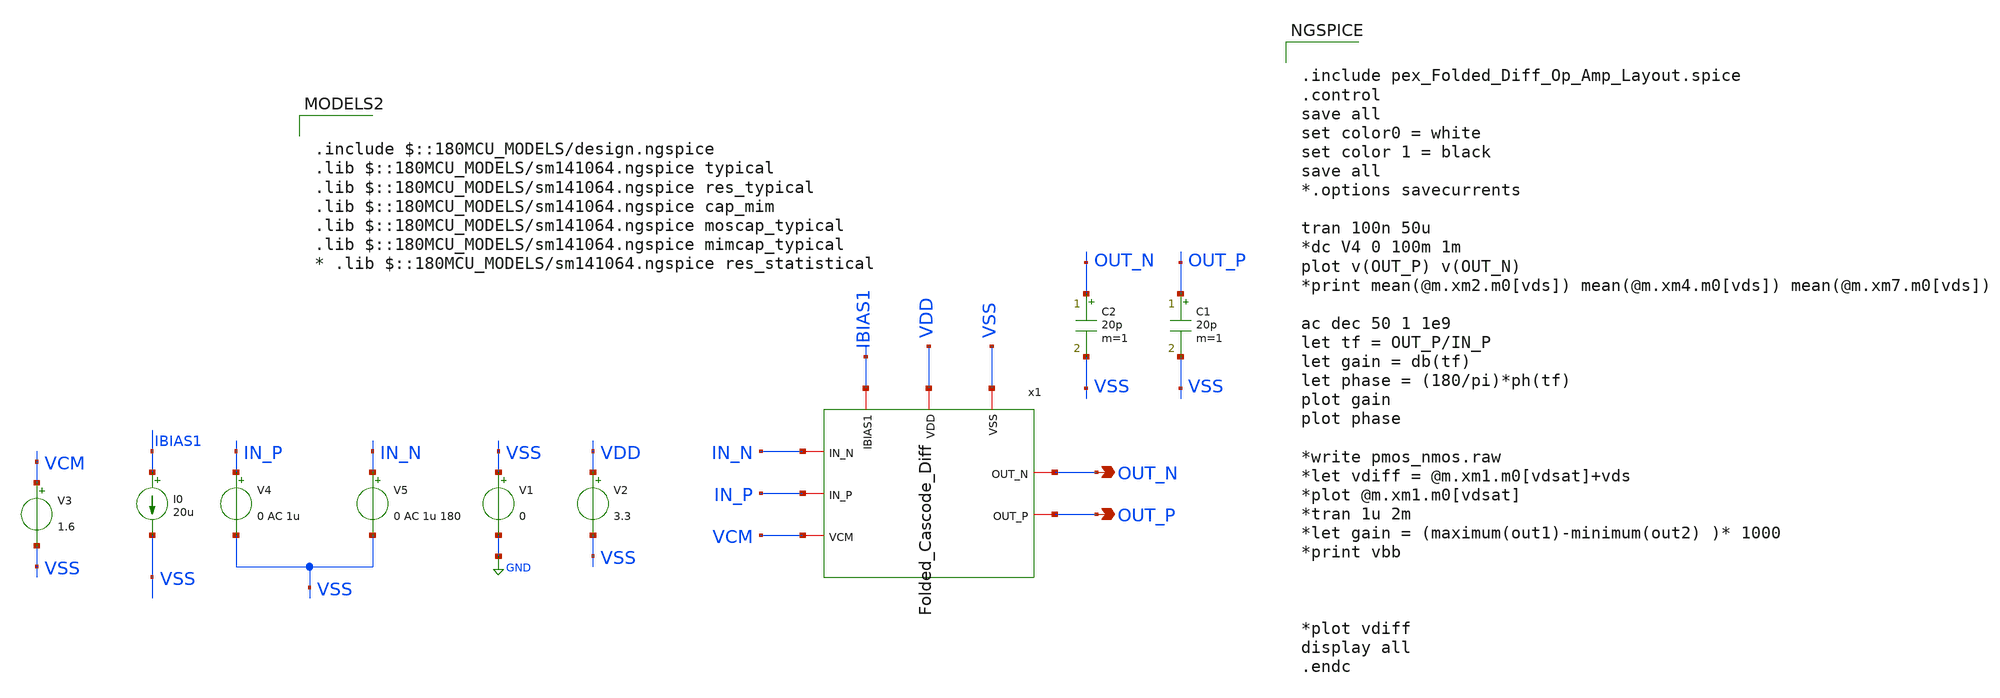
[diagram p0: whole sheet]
** sch_path: AWG_OUTPUT_AND_MUX_PAKISTAN_05/xschem/Folded_Cascode_Diff_TB_Sch.sch
**.subckt Folded_Cascode_Diff_TB_Sch OUT_N OUT_P
*.opin OUT_N
*.opin OUT_P
V1 VSS GND 0
V2 VDD VSS 3.3
V3 VCM VSS 1.6
I0 IBIAS1 VSS 20u
V4 IN_P VSS 0 AC 1u
V5 IN_N VSS 0 AC 1u 180
C1 OUT_P VSS 20p m=1
C2 OUT_N VSS 20p m=1
x1 VDD VSS IN_N IN_P IBIAS1 VCM OUT_N OUT_P Folded_Cascode_Diff
**** begin user architecture code


.include pex_Folded_Diff_Op_Amp_Layout.spice
.control
save all
set color0 = white
set color 1 = black
save all
*.options savecurrents

tran 100n 50u
*dc V4 0 100m 1m
plot v(OUT_P) v(OUT_N)
*print mean(@m.xm2.m0[vds]) mean(@m.xm4.m0[vds]) mean(@m.xm7.m0[vds])

ac dec 50 1 1e9
let tf = OUT_P/IN_P
let gain = db(tf)
let phase = (180/pi)*ph(tf)
plot gain
plot phase

*write pmos_nmos.raw
*let vdiff = @m.xm1.m0[vdsat]+vds
*plot @m.xm1.m0[vdsat]
*tran 1u 2m
*let gain = (maximum(out1)-minimum(out2) )* 1000
*print vbb



*plot vdiff
display all
.endc



.include $::180MCU_MODELS/design.ngspice
.lib $::180MCU_MODELS/sm141064.ngspice typical
.lib $::180MCU_MODELS/sm141064.ngspice res_typical
.lib $::180MCU_MODELS/sm141064.ngspice cap_mim
.lib $::180MCU_MODELS/sm141064.ngspice moscap_typical
.lib $::180MCU_MODELS/sm141064.ngspice mimcap_typical
* .lib $::180MCU_MODELS/sm141064.ngspice res_statistical

**** end user architecture code
**.ends

* expanding   symbol:  Folded_Cascode_Diff.sym # of pins=8
** sym_path: AWG_OUTPUT_AND_MUX_PAKISTAN_05/xschem/Folded_Cascode_Diff.sym
** sch_path: AWG_OUTPUT_AND_MUX_PAKISTAN_05/xschem/Folded_Cascode_Diff.sch
.subckt Folded_Cascode_Diff VDD VSS IN_N IN_P IBIAS1 VCM OUT_N OUT_P
*.iopin VDD
*.iopin VSS
*.iopin IN_N
*.iopin IN_P
*.iopin IBIAS1
*.iopin VCM
*.iopin OUT_N
*.iopin OUT_P
XM1 VPD VB1 VDD VDD pfet_03v3 L=0.28u W=50u nf=1 ad='int((nf+1)/2) * W/nf * 0.18u' as='int((nf+2)/2) * W/nf * 0.18u'
+ pd='2*int((nf+1)/2) * (W/nf + 0.18u)' ps='2*int((nf+2)/2) * (W/nf + 0.18u)' nrd='0.18u / W' nrs='0.18u / W'
+ sa=0 sb=0 sd=0 m=1
XM2 VND VB1 VDD VDD pfet_03v3 L=0.28u W=50u nf=1 ad='int((nf+1)/2) * W/nf * 0.18u' as='int((nf+2)/2) * W/nf * 0.18u'
+ pd='2*int((nf+1)/2) * (W/nf + 0.18u)' ps='2*int((nf+2)/2) * (W/nf + 0.18u)' nrd='0.18u / W' nrs='0.18u / W'
+ sa=0 sb=0 sd=0 m=1
XM3 OUT1 VB2 VND VDD pfet_03v3 L=0.28u W=50u nf=1 ad='int((nf+1)/2) * W/nf * 0.18u' as='int((nf+2)/2) * W/nf * 0.18u'
+ pd='2*int((nf+1)/2) * (W/nf + 0.18u)' ps='2*int((nf+2)/2) * (W/nf + 0.18u)' nrd='0.18u / W' nrs='0.18u / W'
+ sa=0 sb=0 sd=0 m=1
XM4 OUT2 VB2 VPD VDD pfet_03v3 L=0.28u W=50u nf=1 ad='int((nf+1)/2) * W/nf * 0.18u' as='int((nf+2)/2) * W/nf * 0.18u'
+ pd='2*int((nf+1)/2) * (W/nf + 0.18u)' ps='2*int((nf+2)/2) * (W/nf + 0.18u)' nrd='0.18u / W' nrs='0.18u / W'
+ sa=0 sb=0 sd=0 m=1
XM5 OUT2 VB3 IPD VSS nfet_03v3 L=0.28u W=46u nf=1 ad='int((nf+1)/2) * W/nf * 0.18u' as='int((nf+2)/2) * W/nf * 0.18u'
+ pd='2*int((nf+1)/2) * (W/nf + 0.18u)' ps='2*int((nf+2)/2) * (W/nf + 0.18u)' nrd='0.18u / W' nrs='0.18u / W'
+ sa=0 sb=0 sd=0 m=1
XM6 OUT1 VB3 IND VSS nfet_03v3 L=0.28u W=46u nf=1 ad='int((nf+1)/2) * W/nf * 0.18u' as='int((nf+2)/2) * W/nf * 0.18u'
+ pd='2*int((nf+1)/2) * (W/nf + 0.18u)' ps='2*int((nf+2)/2) * (W/nf + 0.18u)' nrd='0.18u / W' nrs='0.18u / W'
+ sa=0 sb=0 sd=0 m=1
XM7 IPD VB4 VSS VSS nfet_03v3 L=0.28u W=92u nf=1 ad='int((nf+1)/2) * W/nf * 0.18u' as='int((nf+2)/2) * W/nf * 0.18u'
+ pd='2*int((nf+1)/2) * (W/nf + 0.18u)' ps='2*int((nf+2)/2) * (W/nf + 0.18u)' nrd='0.18u / W' nrs='0.18u / W'
+ sa=0 sb=0 sd=0 m=1
XM8 IND VB4 VSS VSS nfet_03v3 L=0.28u W=92u nf=1 ad='int((nf+1)/2) * W/nf * 0.18u' as='int((nf+2)/2) * W/nf * 0.18u'
+ pd='2*int((nf+1)/2) * (W/nf + 0.18u)' ps='2*int((nf+2)/2) * (W/nf + 0.18u)' nrd='0.18u / W' nrs='0.18u / W'
+ sa=0 sb=0 sd=0 m=1
XM9 BD IBIAS VDD VDD pfet_03v3 L=0.56u W=100u nf=1 ad='int((nf+1)/2) * W/nf * 0.18u' as='int((nf+2)/2) * W/nf * 0.18u'
+ pd='2*int((nf+1)/2) * (W/nf + 0.18u)' ps='2*int((nf+2)/2) * (W/nf + 0.18u)' nrd='0.18u / W' nrs='0.18u / W'
+ sa=0 sb=0 sd=0 m=1
XM10 IPD IN_P BD VDD pfet_03v3 L=0.28u W=90u nf=1 ad='int((nf+1)/2) * W/nf * 0.18u' as='int((nf+2)/2) * W/nf * 0.18u'
+ pd='2*int((nf+1)/2) * (W/nf + 0.18u)' ps='2*int((nf+2)/2) * (W/nf + 0.18u)' nrd='0.18u / W' nrs='0.18u / W'
+ sa=0 sb=0 sd=0 m=1
XM11 IND IN_N BD VDD pfet_03v3 L=0.28u W=90u nf=1 ad='int((nf+1)/2) * W/nf * 0.18u' as='int((nf+2)/2) * W/nf * 0.18u'
+ pd='2*int((nf+1)/2) * (W/nf + 0.18u)' ps='2*int((nf+2)/2) * (W/nf + 0.18u)' nrd='0.18u / W' nrs='0.18u / W'
+ sa=0 sb=0 sd=0 m=1
XM53 VDD VDD VDD VDD pfet_03v3 L=0.56u W=25.04u nf=1 ad='int((nf+1)/2) * W/nf * 0.18u' as='int((nf+2)/2) * W/nf * 0.18u'
+ pd='2*int((nf+1)/2) * (W/nf + 0.18u)' ps='2*int((nf+2)/2) * (W/nf + 0.18u)' nrd='0.18u / W' nrs='0.18u / W'
+ sa=0 sb=0 sd=0 m=1
XM13 IBS IBIAS1 VDD VDD pfet_03v3 L=0.56u W=20u nf=1 ad='int((nf+1)/2) * W/nf * 0.18u' as='int((nf+2)/2) * W/nf * 0.18u'
+ pd='2*int((nf+1)/2) * (W/nf + 0.18u)' ps='2*int((nf+2)/2) * (W/nf + 0.18u)' nrd='0.18u / W' nrs='0.18u / W'
+ sa=0 sb=0 sd=0 m=1
XM14 IBS IBS VSS VSS nfet_03v3 L=1u W=2u nf=1 ad='int((nf+1)/2) * W/nf * 0.18u' as='int((nf+2)/2) * W/nf * 0.18u'
+ pd='2*int((nf+1)/2) * (W/nf + 0.18u)' ps='2*int((nf+2)/2) * (W/nf + 0.18u)' nrd='0.18u / W' nrs='0.18u / W'
+ sa=0 sb=0 sd=0 m=1
XM15 IBIAS IBS VSS VSS nfet_03v3 L=1u W=2u nf=1 ad='int((nf+1)/2) * W/nf * 0.18u' as='int((nf+2)/2) * W/nf * 0.18u'
+ pd='2*int((nf+1)/2) * (W/nf + 0.18u)' ps='2*int((nf+2)/2) * (W/nf + 0.18u)' nrd='0.18u / W' nrs='0.18u / W'
+ sa=0 sb=0 sd=0 m=1
XM16 IBIAS IBIAS VDD VDD pfet_03v3 L=0.56u W=20u nf=1 ad='int((nf+1)/2) * W/nf * 0.18u' as='int((nf+2)/2) * W/nf * 0.18u'
+ pd='2*int((nf+1)/2) * (W/nf + 0.18u)' ps='2*int((nf+2)/2) * (W/nf + 0.18u)' nrd='0.18u / W' nrs='0.18u / W'
+ sa=0 sb=0 sd=0 m=1
XM17 IBIAS1 IBIAS1 VDD VDD pfet_03v3 L=0.56u W=4u nf=1 ad='int((nf+1)/2) * W/nf * 0.18u' as='int((nf+2)/2) * W/nf * 0.18u'
+ pd='2*int((nf+1)/2) * (W/nf + 0.18u)' ps='2*int((nf+2)/2) * (W/nf + 0.18u)' nrd='0.18u / W' nrs='0.18u / W'
+ sa=0 sb=0 sd=0 m=1
XM19 VBIASN IBIAS1 VDD VDD pfet_03v3 L=0.56u W=4u nf=1 ad='int((nf+1)/2) * W/nf * 0.18u' as='int((nf+2)/2) * W/nf * 0.18u'
+ pd='2*int((nf+1)/2) * (W/nf + 0.18u)' ps='2*int((nf+2)/2) * (W/nf + 0.18u)' nrd='0.18u / W' nrs='0.18u / W'
+ sa=0 sb=0 sd=0 m=1
XM20 VBIASN VBIASN VSS VSS nfet_03v3 L=0.56u W=2u nf=1 ad='int((nf+1)/2) * W/nf * 0.18u' as='int((nf+2)/2) * W/nf * 0.18u'
+ pd='2*int((nf+1)/2) * (W/nf + 0.18u)' ps='2*int((nf+2)/2) * (W/nf + 0.18u)' nrd='0.18u / W' nrs='0.18u / W'
+ sa=0 sb=0 sd=0 m=1
XM26 IB2 VB2 VDD VDD pfet_03v3 L=1u W=0.5u nf=1 ad='int((nf+1)/2) * W/nf * 0.18u' as='int((nf+2)/2) * W/nf * 0.18u'
+ pd='2*int((nf+1)/2) * (W/nf + 0.18u)' ps='2*int((nf+2)/2) * (W/nf + 0.18u)' nrd='0.18u / W' nrs='0.18u / W'
+ sa=0 sb=0 sd=0 m=1
XM27 VB2 VB2 IB2 VDD pfet_03v3 L=0.28u W=8u nf=1 ad='int((nf+1)/2) * W/nf * 0.18u' as='int((nf+2)/2) * W/nf * 0.18u'
+ pd='2*int((nf+1)/2) * (W/nf + 0.18u)' ps='2*int((nf+2)/2) * (W/nf + 0.18u)' nrd='0.18u / W' nrs='0.18u / W'
+ sa=0 sb=0 sd=0 m=1
XM28 VB2 VBIASN VSS VSS nfet_03v3 L=0.56u W=1u nf=1 ad='int((nf+1)/2) * W/nf * 0.18u' as='int((nf+2)/2) * W/nf * 0.18u'
+ pd='2*int((nf+1)/2) * (W/nf + 0.18u)' ps='2*int((nf+2)/2) * (W/nf + 0.18u)' nrd='0.18u / W' nrs='0.18u / W'
+ sa=0 sb=0 sd=0 m=1
XM21 VCD VBIASN VSS VSS nfet_03v3 L=0.56u W=6u nf=1 ad='int((nf+1)/2) * W/nf * 0.18u' as='int((nf+2)/2) * W/nf * 0.18u'
+ pd='2*int((nf+1)/2) * (W/nf + 0.18u)' ps='2*int((nf+2)/2) * (W/nf + 0.18u)' nrd='0.18u / W' nrs='0.18u / W'
+ sa=0 sb=0 sd=0 m=1
XM22 VBM VCM VCD VSS nfet_03v3 L=0.28u W=30u nf=1 ad='int((nf+1)/2) * W/nf * 0.18u' as='int((nf+2)/2) * W/nf * 0.18u'
+ pd='2*int((nf+1)/2) * (W/nf + 0.18u)' ps='2*int((nf+2)/2) * (W/nf + 0.18u)' nrd='0.18u / W' nrs='0.18u / W'
+ sa=0 sb=0 sd=0 m=1
XM23 VB1 VOUT VCD VSS nfet_03v3 L=0.28u W=30u nf=1 ad='int((nf+1)/2) * W/nf * 0.18u' as='int((nf+2)/2) * W/nf * 0.18u'
+ pd='2*int((nf+1)/2) * (W/nf + 0.18u)' ps='2*int((nf+2)/2) * (W/nf + 0.18u)' nrd='0.18u / W' nrs='0.18u / W'
+ sa=0 sb=0 sd=0 m=1
XM24 VBM VBM VDD VDD pfet_03v3 L=0.28u W=8u nf=1 ad='int((nf+1)/2) * W/nf * 0.18u' as='int((nf+2)/2) * W/nf * 0.18u'
+ pd='2*int((nf+1)/2) * (W/nf + 0.18u)' ps='2*int((nf+2)/2) * (W/nf + 0.18u)' nrd='0.18u / W' nrs='0.18u / W'
+ sa=0 sb=0 sd=0 m=1
XM25 VB1 VB1 VDD VDD pfet_03v3 L=0.28u W=8u nf=1 ad='int((nf+1)/2) * W/nf * 0.18u' as='int((nf+2)/2) * W/nf * 0.18u'
+ pd='2*int((nf+1)/2) * (W/nf + 0.18u)' ps='2*int((nf+2)/2) * (W/nf + 0.18u)' nrd='0.18u / W' nrs='0.18u / W'
+ sa=0 sb=0 sd=0 m=1
XM18 IB5 IBIAS1 VDD VDD pfet_03v3 L=0.56u W=16u nf=1 ad='int((nf+1)/2) * W/nf * 0.18u' as='int((nf+2)/2) * W/nf * 0.18u'
+ pd='2*int((nf+1)/2) * (W/nf + 0.18u)' ps='2*int((nf+2)/2) * (W/nf + 0.18u)' nrd='0.18u / W' nrs='0.18u / W'
+ sa=0 sb=0 sd=0 m=1
XM29 IB5 IB5 VB4 VSS nfet_03v3 L=0.28u W=4u nf=1 ad='int((nf+1)/2) * W/nf * 0.18u' as='int((nf+2)/2) * W/nf * 0.18u'
+ pd='2*int((nf+1)/2) * (W/nf + 0.18u)' ps='2*int((nf+2)/2) * (W/nf + 0.18u)' nrd='0.18u / W' nrs='0.18u / W'
+ sa=0 sb=0 sd=0 m=1
XM30 VB4 VB4 VSS VSS nfet_03v3 L=0.28u W=14u nf=1 ad='int((nf+1)/2) * W/nf * 0.18u' as='int((nf+2)/2) * W/nf * 0.18u'
+ pd='2*int((nf+1)/2) * (W/nf + 0.18u)' ps='2*int((nf+2)/2) * (W/nf + 0.18u)' nrd='0.18u / W' nrs='0.18u / W'
+ sa=0 sb=0 sd=0 m=1
XM32 VB3 IBIAS1 VDD VDD pfet_03v3 L=0.56u W=8u nf=1 ad='int((nf+1)/2) * W/nf * 0.18u' as='int((nf+2)/2) * W/nf * 0.18u'
+ pd='2*int((nf+1)/2) * (W/nf + 0.18u)' ps='2*int((nf+2)/2) * (W/nf + 0.18u)' nrd='0.18u / W' nrs='0.18u / W'
+ sa=0 sb=0 sd=0 m=1
XM33 VB3 VB3 IB3 VSS nfet_03v3 L=0.28u W=7u nf=1 ad='int((nf+1)/2) * W/nf * 0.18u' as='int((nf+2)/2) * W/nf * 0.18u'
+ pd='2*int((nf+1)/2) * (W/nf + 0.18u)' ps='2*int((nf+2)/2) * (W/nf + 0.18u)' nrd='0.18u / W' nrs='0.18u / W'
+ sa=0 sb=0 sd=0 m=1
XM34 IB3 VB3 VSS VSS nfet_03v3 L=0.56u W=1u nf=1 ad='int((nf+1)/2) * W/nf * 0.18u' as='int((nf+2)/2) * W/nf * 0.18u'
+ pd='2*int((nf+1)/2) * (W/nf + 0.18u)' ps='2*int((nf+2)/2) * (W/nf + 0.18u)' nrd='0.18u / W' nrs='0.18u / W'
+ sa=0 sb=0 sd=0 m=1
XM36 OUT_P IBIAS2 VDD VDD pfet_03v3 L=0.28u W=84u nf=1 ad='int((nf+1)/2) * W/nf * 0.18u' as='int((nf+2)/2) * W/nf * 0.18u'
+ pd='2*int((nf+1)/2) * (W/nf + 0.18u)' ps='2*int((nf+2)/2) * (W/nf + 0.18u)' nrd='0.18u / W' nrs='0.18u / W'
+ sa=0 sb=0 sd=0 m=1
XM38 OUT_P OUT2 VSS VSS nfet_03v3 L=0.28u W=72u nf=1 ad='int((nf+1)/2) * W/nf * 0.18u' as='int((nf+2)/2) * W/nf * 0.18u'
+ pd='2*int((nf+1)/2) * (W/nf + 0.18u)' ps='2*int((nf+2)/2) * (W/nf + 0.18u)' nrd='0.18u / W' nrs='0.18u / W'
+ sa=0 sb=0 sd=0 m=1
XM39 OUT_P IBIAS2 VDD VDD pfet_03v3 L=0.28u W=84u nf=1 ad='int((nf+1)/2) * W/nf * 0.18u' as='int((nf+2)/2) * W/nf * 0.18u'
+ pd='2*int((nf+1)/2) * (W/nf + 0.18u)' ps='2*int((nf+2)/2) * (W/nf + 0.18u)' nrd='0.18u / W' nrs='0.18u / W'
+ sa=0 sb=0 sd=0 m=1
XM40 OUT_N IBIAS2 VDD VDD pfet_03v3 L=0.28u W=84u nf=1 ad='int((nf+1)/2) * W/nf * 0.18u' as='int((nf+2)/2) * W/nf * 0.18u'
+ pd='2*int((nf+1)/2) * (W/nf + 0.18u)' ps='2*int((nf+2)/2) * (W/nf + 0.18u)' nrd='0.18u / W' nrs='0.18u / W'
+ sa=0 sb=0 sd=0 m=1
XM41 OUT_N OUT1 VSS VSS nfet_03v3 L=0.28u W=72u nf=1 ad='int((nf+1)/2) * W/nf * 0.18u' as='int((nf+2)/2) * W/nf * 0.18u'
+ pd='2*int((nf+1)/2) * (W/nf + 0.18u)' ps='2*int((nf+2)/2) * (W/nf + 0.18u)' nrd='0.18u / W' nrs='0.18u / W'
+ sa=0 sb=0 sd=0 m=1
XM42 OUT_N IBIAS2 VDD VDD pfet_03v3 L=0.28u W=84u nf=1 ad='int((nf+1)/2) * W/nf * 0.18u' as='int((nf+2)/2) * W/nf * 0.18u'
+ pd='2*int((nf+1)/2) * (W/nf + 0.18u)' ps='2*int((nf+2)/2) * (W/nf + 0.18u)' nrd='0.18u / W' nrs='0.18u / W'
+ sa=0 sb=0 sd=0 m=1
XM43 OUT_N OUT1 VSS VSS nfet_03v3 L=0.28u W=72u nf=1 ad='int((nf+1)/2) * W/nf * 0.18u' as='int((nf+2)/2) * W/nf * 0.18u'
+ pd='2*int((nf+1)/2) * (W/nf + 0.18u)' ps='2*int((nf+2)/2) * (W/nf + 0.18u)' nrd='0.18u / W' nrs='0.18u / W'
+ sa=0 sb=0 sd=0 m=1
XM44 OUT_P OUT2 VSS VSS nfet_03v3 L=0.28u W=72u nf=1 ad='int((nf+1)/2) * W/nf * 0.18u' as='int((nf+2)/2) * W/nf * 0.18u'
+ pd='2*int((nf+1)/2) * (W/nf + 0.18u)' ps='2*int((nf+2)/2) * (W/nf + 0.18u)' nrd='0.18u / W' nrs='0.18u / W'
+ sa=0 sb=0 sd=0 m=1
XM45 OUT_N IBIAS2 VDD VDD pfet_03v3 L=0.28u W=84u nf=1 ad='int((nf+1)/2) * W/nf * 0.18u' as='int((nf+2)/2) * W/nf * 0.18u'
+ pd='2*int((nf+1)/2) * (W/nf + 0.18u)' ps='2*int((nf+2)/2) * (W/nf + 0.18u)' nrd='0.18u / W' nrs='0.18u / W'
+ sa=0 sb=0 sd=0 m=1
XM46 OUT_P IBIAS2 VDD VDD pfet_03v3 L=0.28u W=84u nf=1 ad='int((nf+1)/2) * W/nf * 0.18u' as='int((nf+2)/2) * W/nf * 0.18u'
+ pd='2*int((nf+1)/2) * (W/nf + 0.18u)' ps='2*int((nf+2)/2) * (W/nf + 0.18u)' nrd='0.18u / W' nrs='0.18u / W'
+ sa=0 sb=0 sd=0 m=1
XM47 OUT_P IBIAS2 VDD VDD pfet_03v3 L=0.28u W=84u nf=1 ad='int((nf+1)/2) * W/nf * 0.18u' as='int((nf+2)/2) * W/nf * 0.18u'
+ pd='2*int((nf+1)/2) * (W/nf + 0.18u)' ps='2*int((nf+2)/2) * (W/nf + 0.18u)' nrd='0.18u / W' nrs='0.18u / W'
+ sa=0 sb=0 sd=0 m=1
XM48 OUT_N IBIAS2 VDD VDD pfet_03v3 L=0.28u W=84u nf=1 ad='int((nf+1)/2) * W/nf * 0.18u' as='int((nf+2)/2) * W/nf * 0.18u'
+ pd='2*int((nf+1)/2) * (W/nf + 0.18u)' ps='2*int((nf+2)/2) * (W/nf + 0.18u)' nrd='0.18u / W' nrs='0.18u / W'
+ sa=0 sb=0 sd=0 m=1
XM50 OUT_N OUT1 VSS VSS nfet_03v3 L=0.28u W=72u nf=1 ad='int((nf+1)/2) * W/nf * 0.18u' as='int((nf+2)/2) * W/nf * 0.18u'
+ pd='2*int((nf+1)/2) * (W/nf + 0.18u)' ps='2*int((nf+2)/2) * (W/nf + 0.18u)' nrd='0.18u / W' nrs='0.18u / W'
+ sa=0 sb=0 sd=0 m=1
XM51 OUT_P OUT2 VSS VSS nfet_03v3 L=0.28u W=72u nf=1 ad='int((nf+1)/2) * W/nf * 0.18u' as='int((nf+2)/2) * W/nf * 0.18u'
+ pd='2*int((nf+1)/2) * (W/nf + 0.18u)' ps='2*int((nf+2)/2) * (W/nf + 0.18u)' nrd='0.18u / W' nrs='0.18u / W'
+ sa=0 sb=0 sd=0 m=1
XM52 OUT_P IBIAS2 VDD VDD pfet_03v3 L=0.28u W=84u nf=1 ad='int((nf+1)/2) * W/nf * 0.18u' as='int((nf+2)/2) * W/nf * 0.18u'
+ pd='2*int((nf+1)/2) * (W/nf + 0.18u)' ps='2*int((nf+2)/2) * (W/nf + 0.18u)' nrd='0.18u / W' nrs='0.18u / W'
+ sa=0 sb=0 sd=0 m=1
XM54 OUT_N IBIAS2 VDD VDD pfet_03v3 L=0.28u W=84u nf=1 ad='int((nf+1)/2) * W/nf * 0.18u' as='int((nf+2)/2) * W/nf * 0.18u'
+ pd='2*int((nf+1)/2) * (W/nf + 0.18u)' ps='2*int((nf+2)/2) * (W/nf + 0.18u)' nrd='0.18u / W' nrs='0.18u / W'
+ sa=0 sb=0 sd=0 m=1
XM55 OUT_N IBIAS2 VDD VDD pfet_03v3 L=0.28u W=84u nf=1 ad='int((nf+1)/2) * W/nf * 0.18u' as='int((nf+2)/2) * W/nf * 0.18u'
+ pd='2*int((nf+1)/2) * (W/nf + 0.18u)' ps='2*int((nf+2)/2) * (W/nf + 0.18u)' nrd='0.18u / W' nrs='0.18u / W'
+ sa=0 sb=0 sd=0 m=1
XM57 OUT_P IBIAS2 VDD VDD pfet_03v3 L=0.28u W=84u nf=1 ad='int((nf+1)/2) * W/nf * 0.18u' as='int((nf+2)/2) * W/nf * 0.18u'
+ pd='2*int((nf+1)/2) * (W/nf + 0.18u)' ps='2*int((nf+2)/2) * (W/nf + 0.18u)' nrd='0.18u / W' nrs='0.18u / W'
+ sa=0 sb=0 sd=0 m=1
XM68 IBIAS2 IBIAS2 VDD VDD pfet_03v3 L=0.28u W=84u nf=1 ad='int((nf+1)/2) * W/nf * 0.18u' as='int((nf+2)/2) * W/nf * 0.18u'
+ pd='2*int((nf+1)/2) * (W/nf + 0.18u)' ps='2*int((nf+2)/2) * (W/nf + 0.18u)' nrd='0.18u / W' nrs='0.18u / W'
+ sa=0 sb=0 sd=0 m=1
XM69 IBIAS2 IBIAS2 VDD VDD pfet_03v3 L=0.28u W=84u nf=1 ad='int((nf+1)/2) * W/nf * 0.18u' as='int((nf+2)/2) * W/nf * 0.18u'
+ pd='2*int((nf+1)/2) * (W/nf + 0.18u)' ps='2*int((nf+2)/2) * (W/nf + 0.18u)' nrd='0.18u / W' nrs='0.18u / W'
+ sa=0 sb=0 sd=0 m=1
XM70 IVS IBIAS3 VDD VDD pfet_03v3 L=0.28u W=84u nf=1 ad='int((nf+1)/2) * W/nf * 0.18u' as='int((nf+2)/2) * W/nf * 0.18u'
+ pd='2*int((nf+1)/2) * (W/nf + 0.18u)' ps='2*int((nf+2)/2) * (W/nf + 0.18u)' nrd='0.18u / W' nrs='0.18u / W'
+ sa=0 sb=0 sd=0 m=1
XM71 IVS IVS VSS VSS nfet_03v3 L=1u W=20u nf=1 ad='int((nf+1)/2) * W/nf * 0.18u' as='int((nf+2)/2) * W/nf * 0.18u'
+ pd='2*int((nf+1)/2) * (W/nf + 0.18u)' ps='2*int((nf+2)/2) * (W/nf + 0.18u)' nrd='0.18u / W' nrs='0.18u / W'
+ sa=0 sb=0 sd=0 m=1
XM72 IBIAS2 IVS VSS VSS nfet_03v3 L=1u W=20u nf=1 ad='int((nf+1)/2) * W/nf * 0.18u' as='int((nf+2)/2) * W/nf * 0.18u'
+ pd='2*int((nf+1)/2) * (W/nf + 0.18u)' ps='2*int((nf+2)/2) * (W/nf + 0.18u)' nrd='0.18u / W' nrs='0.18u / W'
+ sa=0 sb=0 sd=0 m=1
XM73 IVS IBIAS3 VDD VDD pfet_03v3 L=0.28u W=84u nf=1 ad='int((nf+1)/2) * W/nf * 0.18u' as='int((nf+2)/2) * W/nf * 0.18u'
+ pd='2*int((nf+1)/2) * (W/nf + 0.18u)' ps='2*int((nf+2)/2) * (W/nf + 0.18u)' nrd='0.18u / W' nrs='0.18u / W'
+ sa=0 sb=0 sd=0 m=1
XM76 IBIAS3 IBIAS3 VDD VDD pfet_03v3 L=0.28u W=24u nf=1 ad='int((nf+1)/2) * W/nf * 0.18u' as='int((nf+2)/2) * W/nf * 0.18u'
+ pd='2*int((nf+1)/2) * (W/nf + 0.18u)' ps='2*int((nf+2)/2) * (W/nf + 0.18u)' nrd='0.18u / W' nrs='0.18u / W'
+ sa=0 sb=0 sd=0 m=1
XM77 IB4 IBIAS4 VDD VDD pfet_03v3 L=0.28u W=24u nf=1 ad='int((nf+1)/2) * W/nf * 0.18u' as='int((nf+2)/2) * W/nf * 0.18u'
+ pd='2*int((nf+1)/2) * (W/nf + 0.18u)' ps='2*int((nf+2)/2) * (W/nf + 0.18u)' nrd='0.18u / W' nrs='0.18u / W'
+ sa=0 sb=0 sd=0 m=1
XM78 IB4 IB4 VSS VSS nfet_03v3 L=1u W=10u nf=1 ad='int((nf+1)/2) * W/nf * 0.18u' as='int((nf+2)/2) * W/nf * 0.18u'
+ pd='2*int((nf+1)/2) * (W/nf + 0.18u)' ps='2*int((nf+2)/2) * (W/nf + 0.18u)' nrd='0.18u / W' nrs='0.18u / W'
+ sa=0 sb=0 sd=0 m=1
XM79 IBIAS3 IB4 VSS VSS nfet_03v3 L=1u W=10u nf=1 ad='int((nf+1)/2) * W/nf * 0.18u' as='int((nf+2)/2) * W/nf * 0.18u'
+ pd='2*int((nf+1)/2) * (W/nf + 0.18u)' ps='2*int((nf+2)/2) * (W/nf + 0.18u)' nrd='0.18u / W' nrs='0.18u / W'
+ sa=0 sb=0 sd=0 m=1
XM80 IBIAS4 IBIAS4 VDD VDD pfet_03v3 L=0.28u W=5u nf=1 ad='int((nf+1)/2) * W/nf * 0.18u' as='int((nf+2)/2) * W/nf * 0.18u'
+ pd='2*int((nf+1)/2) * (W/nf + 0.18u)' ps='2*int((nf+2)/2) * (W/nf + 0.18u)' nrd='0.18u / W' nrs='0.18u / W'
+ sa=0 sb=0 sd=0 m=1
XM81 IBIAS4 VBIASN VSS VSS nfet_03v3 L=1u W=2u nf=1 ad='int((nf+1)/2) * W/nf * 0.18u' as='int((nf+2)/2) * W/nf * 0.18u'
+ pd='2*int((nf+1)/2) * (W/nf + 0.18u)' ps='2*int((nf+2)/2) * (W/nf + 0.18u)' nrd='0.18u / W' nrs='0.18u / W'
+ sa=0 sb=0 sd=0 m=1
XR21 VDD VDD VDD ppolyf_u r_width=4e-6 r_length=6.2e-6 m=1
XR1 net2 OUT_P VDD ppolyf_u r_width=1e-6 r_length=5e-6 m=1
XR2 net2 net1 VDD ppolyf_u r_width=1e-6 r_length=5e-6 m=1
XR3 net3 net1 VDD ppolyf_u r_width=1e-6 r_length=5e-6 m=1
XR4 net3 net4 VDD ppolyf_u r_width=1e-6 r_length=5e-6 m=1
XR5 net5 net4 VDD ppolyf_u r_width=1e-6 r_length=5e-6 m=1
XR6 net5 net6 VDD ppolyf_u r_width=1e-6 r_length=5e-6 m=1
XR7 net7 net6 VDD ppolyf_u r_width=1e-6 r_length=5e-6 m=1
XR8 net7 net8 VDD ppolyf_u r_width=1e-6 r_length=5e-6 m=1
XR9 net9 net8 VDD ppolyf_u r_width=1e-6 r_length=5e-6 m=1
XR10 net9 VOUT VDD ppolyf_u r_width=1e-6 r_length=5e-6 m=1
XR11 net11 OUT_N VDD ppolyf_u r_width=1e-6 r_length=5e-6 m=1
XR12 net11 net10 VDD ppolyf_u r_width=1e-6 r_length=5e-6 m=1
XR13 net12 net10 VDD ppolyf_u r_width=1e-6 r_length=5e-6 m=1
XR14 net12 net13 VDD ppolyf_u r_width=1e-6 r_length=5e-6 m=1
XR15 net14 net13 VDD ppolyf_u r_width=1e-6 r_length=5e-6 m=1
XR16 net14 net15 VDD ppolyf_u r_width=1e-6 r_length=5e-6 m=1
XR17 net16 net15 VDD ppolyf_u r_width=1e-6 r_length=5e-6 m=1
XR18 net16 net17 VDD ppolyf_u r_width=1e-6 r_length=5e-6 m=1
XR19 net18 net17 VDD ppolyf_u r_width=1e-6 r_length=5e-6 m=1
XR20 net18 VOUT VDD ppolyf_u r_width=1e-6 r_length=5e-6 m=1
XR22 VOUT1 OUT1 VDD ppolyf_u r_width=1e-6 r_length=6.2e-6 m=1
XR23 VOUT2 OUT2 VDD ppolyf_u r_width=1e-6 r_length=6.2e-6 m=1
XR24 VOUT1 OUT1 VDD ppolyf_u r_width=1e-6 r_length=6.2e-6 m=1
XR25 VOUT2 OUT2 VDD ppolyf_u r_width=1e-6 r_length=6.2e-6 m=1
XR26 VOUT1 OUT1 VDD ppolyf_u r_width=1e-6 r_length=6.2e-6 m=1
XR27 VOUT2 OUT2 VDD ppolyf_u r_width=1e-6 r_length=6.2e-6 m=1
XR28 VOUT1 OUT1 VDD ppolyf_u r_width=1e-6 r_length=6.2e-6 m=1
XR29 VOUT2 OUT2 VDD ppolyf_u r_width=1e-6 r_length=6.2e-6 m=1
XR30 VDD VDD VDD ppolyf_u r_width=4e-6 r_length=5e-6 m=1
XC1 VOUT1 OUT_N cap_mim_2f0_m4m5_noshield c_width=21e-6 c_length=21e-6 m=1
XC2 VOUT2 OUT_P cap_mim_2f0_m4m5_noshield c_width=21e-6 c_length=21e-6 m=1
XC4 VOUT1 OUT_N cap_mim_2f0_m4m5_noshield c_width=21e-6 c_length=21e-6 m=1
XC5 VOUT2 OUT_P cap_mim_2f0_m4m5_noshield c_width=21e-6 c_length=21e-6 m=1
XM82 OUT_N IBIAS2 VDD VDD pfet_03v3 L=0.28u W=84u nf=1 ad='int((nf+1)/2) * W/nf * 0.18u' as='int((nf+2)/2) * W/nf * 0.18u'
+ pd='2*int((nf+1)/2) * (W/nf + 0.18u)' ps='2*int((nf+2)/2) * (W/nf + 0.18u)' nrd='0.18u / W' nrs='0.18u / W'
+ sa=0 sb=0 sd=0 m=1
XM83 OUT_P IBIAS2 VDD VDD pfet_03v3 L=0.28u W=84u nf=1 ad='int((nf+1)/2) * W/nf * 0.18u' as='int((nf+2)/2) * W/nf * 0.18u'
+ pd='2*int((nf+1)/2) * (W/nf + 0.18u)' ps='2*int((nf+2)/2) * (W/nf + 0.18u)' nrd='0.18u / W' nrs='0.18u / W'
+ sa=0 sb=0 sd=0 m=1
XM12 VDD VDD VDD VDD pfet_03v3 L=0.28u W=45u nf=1 ad='int((nf+1)/2) * W/nf * 0.18u' as='int((nf+2)/2) * W/nf * 0.18u'
+ pd='2*int((nf+1)/2) * (W/nf + 0.18u)' ps='2*int((nf+2)/2) * (W/nf + 0.18u)' nrd='0.18u / W' nrs='0.18u / W'
+ sa=0 sb=0 sd=0 m=1
XM31 VDD VDD VDD VDD pfet_03v3 L=0.28u W=25.04u nf=1 ad='int((nf+1)/2) * W/nf * 0.18u' as='int((nf+2)/2) * W/nf * 0.18u'
+ pd='2*int((nf+1)/2) * (W/nf + 0.18u)' ps='2*int((nf+2)/2) * (W/nf + 0.18u)' nrd='0.18u / W' nrs='0.18u / W'
+ sa=0 sb=0 sd=0 m=1
XM35 VDD VDD VDD VDD pfet_03v3 L=0.28u W=25.04u nf=1 ad='int((nf+1)/2) * W/nf * 0.18u' as='int((nf+2)/2) * W/nf * 0.18u'
+ pd='2*int((nf+1)/2) * (W/nf + 0.18u)' ps='2*int((nf+2)/2) * (W/nf + 0.18u)' nrd='0.18u / W' nrs='0.18u / W'
+ sa=0 sb=0 sd=0 m=1
XM37 VDD VDD VDD VDD pfet_03v3 L=0.28u W=24u nf=1 ad='int((nf+1)/2) * W/nf * 0.18u' as='int((nf+2)/2) * W/nf * 0.18u'
+ pd='2*int((nf+1)/2) * (W/nf + 0.18u)' ps='2*int((nf+2)/2) * (W/nf + 0.18u)' nrd='0.18u / W' nrs='0.18u / W'
+ sa=0 sb=0 sd=0 m=1
XM49 VDD VDD VDD VDD pfet_03v3 L=0.28u W=24u nf=1 ad='int((nf+1)/2) * W/nf * 0.18u' as='int((nf+2)/2) * W/nf * 0.18u'
+ pd='2*int((nf+1)/2) * (W/nf + 0.18u)' ps='2*int((nf+2)/2) * (W/nf + 0.18u)' nrd='0.18u / W' nrs='0.18u / W'
+ sa=0 sb=0 sd=0 m=1
XM56 VDD VDD VDD VDD pfet_03v3 L=0.28u W=24u nf=1 ad='int((nf+1)/2) * W/nf * 0.18u' as='int((nf+2)/2) * W/nf * 0.18u'
+ pd='2*int((nf+1)/2) * (W/nf + 0.18u)' ps='2*int((nf+2)/2) * (W/nf + 0.18u)' nrd='0.18u / W' nrs='0.18u / W'
+ sa=0 sb=0 sd=0 m=1
XM58 VDD VDD VDD VDD pfet_03v3 L=0.28u W=24u nf=1 ad='int((nf+1)/2) * W/nf * 0.18u' as='int((nf+2)/2) * W/nf * 0.18u'
+ pd='2*int((nf+1)/2) * (W/nf + 0.18u)' ps='2*int((nf+2)/2) * (W/nf + 0.18u)' nrd='0.18u / W' nrs='0.18u / W'
+ sa=0 sb=0 sd=0 m=1
XM59 VDD VDD VDD VDD pfet_03v3 L=0.28u W=24u nf=1 ad='int((nf+1)/2) * W/nf * 0.18u' as='int((nf+2)/2) * W/nf * 0.18u'
+ pd='2*int((nf+1)/2) * (W/nf + 0.18u)' ps='2*int((nf+2)/2) * (W/nf + 0.18u)' nrd='0.18u / W' nrs='0.18u / W'
+ sa=0 sb=0 sd=0 m=1
XM60 VDD VDD VDD VDD pfet_03v3 L=0.28u W=24u nf=1 ad='int((nf+1)/2) * W/nf * 0.18u' as='int((nf+2)/2) * W/nf * 0.18u'
+ pd='2*int((nf+1)/2) * (W/nf + 0.18u)' ps='2*int((nf+2)/2) * (W/nf + 0.18u)' nrd='0.18u / W' nrs='0.18u / W'
+ sa=0 sb=0 sd=0 m=1
XM61 VDD VDD VDD VDD pfet_03v3 L=0.28u W=24u nf=1 ad='int((nf+1)/2) * W/nf * 0.18u' as='int((nf+2)/2) * W/nf * 0.18u'
+ pd='2*int((nf+1)/2) * (W/nf + 0.18u)' ps='2*int((nf+2)/2) * (W/nf + 0.18u)' nrd='0.18u / W' nrs='0.18u / W'
+ sa=0 sb=0 sd=0 m=1
XM62 VDD VDD VDD VDD pfet_03v3 L=0.28u W=32u nf=1 ad='int((nf+1)/2) * W/nf * 0.18u' as='int((nf+2)/2) * W/nf * 0.18u'
+ pd='2*int((nf+1)/2) * (W/nf + 0.18u)' ps='2*int((nf+2)/2) * (W/nf + 0.18u)' nrd='0.18u / W' nrs='0.18u / W'
+ sa=0 sb=0 sd=0 m=1
XM74 VDD VDD VDD VDD pfet_03v3 L=0.28u W=1u nf=1 ad='int((nf+1)/2) * W/nf * 0.18u' as='int((nf+2)/2) * W/nf * 0.18u'
+ pd='2*int((nf+1)/2) * (W/nf + 0.18u)' ps='2*int((nf+2)/2) * (W/nf + 0.18u)' nrd='0.18u / W' nrs='0.18u / W'
+ sa=0 sb=0 sd=0 m=1
XM84 VDD VDD VDD VDD pfet_03v3 L=0.28u W=30u nf=1 ad='int((nf+1)/2) * W/nf * 0.18u' as='int((nf+2)/2) * W/nf * 0.18u'
+ pd='2*int((nf+1)/2) * (W/nf + 0.18u)' ps='2*int((nf+2)/2) * (W/nf + 0.18u)' nrd='0.18u / W' nrs='0.18u / W'
+ sa=0 sb=0 sd=0 m=1
.ends

.GLOBAL GND
.end
